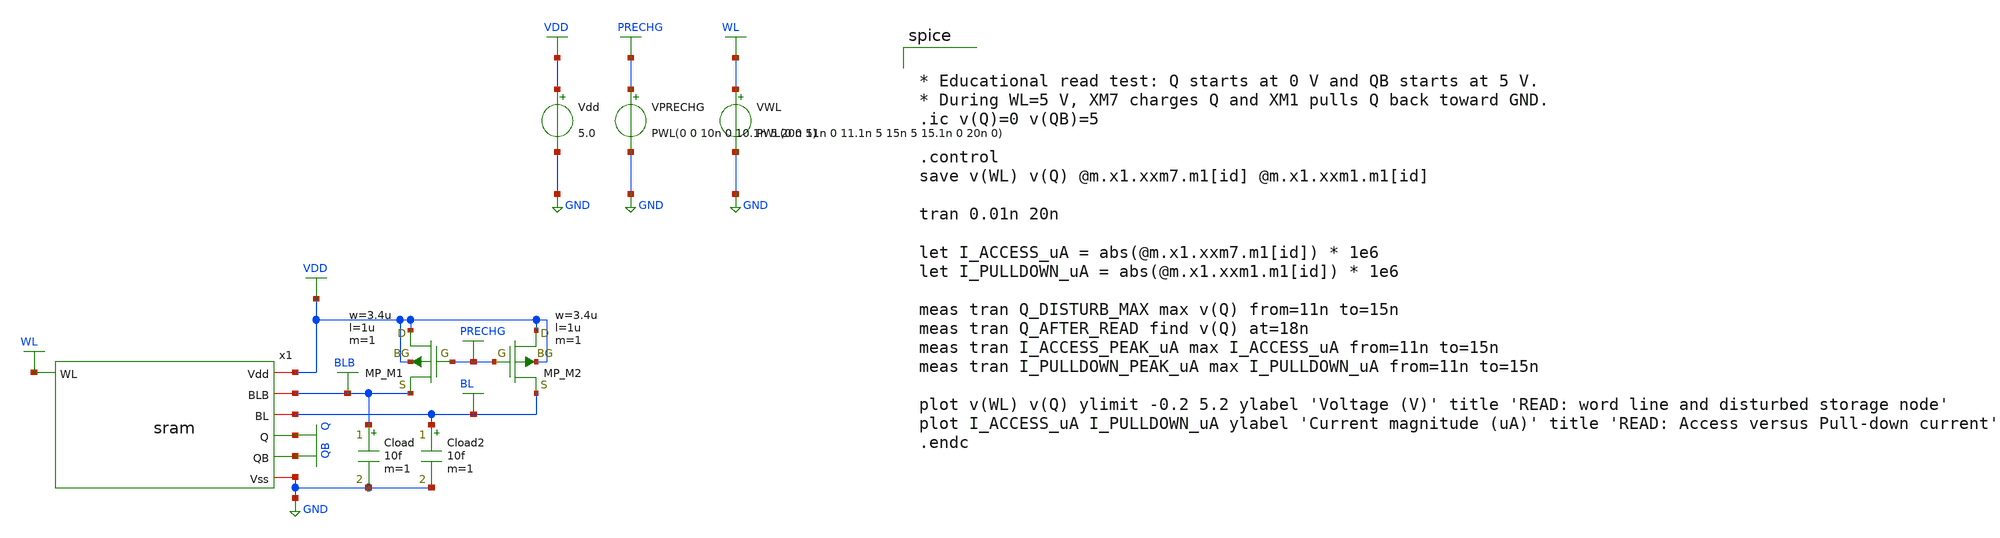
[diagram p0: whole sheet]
** sch_path: sram_tb_read_strength.sch
**.subckt sram_tb_read_strength
Vdd VDD GND 5.0
VWL WL GND PWL(0 0 11n 0 11.1n 5 15n 5 15.1n 0 20n 0)
x1 WL VDD BLB BL Q QB GND sram
XM1 VDD PRECHG BLB VDD PMOS w=3.4u l=1u as=0 ad=0 ps=0 pd=0 nrd=0 nrs=0 m=1
XM2 VDD PRECHG BL VDD PMOS w=3.4u l=1u as=0 ad=0 ps=0 pd=0 nrd=0 nrs=0 m=1
Cload BLB GND 10f m=1
Cload2 BL GND 10f m=1
VPRECHG PRECHG GND PWL(0 0 10n 0 10.1n 5 20n 5)
**** begin user architecture code
 .include $::LIB/ip62_models


* Educational read test: Q starts at 0 V and QB starts at 5 V.
* During WL=5 V, XM7 charges Q and XM1 pulls Q back toward GND.
.ic v(Q)=0 v(QB)=5

.control
save v(WL) v(Q) @m.x1.xxm7.m1[id] @m.x1.xxm1.m1[id]

tran 0.01n 20n

let I_ACCESS_uA = abs(@m.x1.xxm7.m1[id]) * 1e6
let I_PULLDOWN_uA = abs(@m.x1.xxm1.m1[id]) * 1e6

meas tran Q_DISTURB_MAX max v(Q) from=11n to=15n
meas tran Q_AFTER_READ find v(Q) at=18n
meas tran I_ACCESS_PEAK_uA max I_ACCESS_uA from=11n to=15n
meas tran I_PULLDOWN_PEAK_uA max I_PULLDOWN_uA from=11n to=15n

plot v(WL) v(Q) ylimit -0.2 5.2 ylabel 'Voltage (V)' title 'READ: word line and disturbed storage node'
plot I_ACCESS_uA I_PULLDOWN_uA ylabel 'Current magnitude (uA)' title 'READ: Access versus Pull-down current'
.endc


**** end user architecture code
**.ends

* expanding   symbol:  sram.sym # of pins=7
** sym_path: sram.sym
** sch_path: sram.sch
.subckt sram WL Vdd BLB BL Q QB Vss
*.iopin Vdd
*.iopin Vss
*.iopin BLB
*.iopin BL
*.ipin WL
*.opin Q
*.opin QB
XXM1 Q QB Vss Vss NMOS w=3.4u l=1u nrd=0 nrs=0 m=1
XXM2 Q QB Vdd Vdd PMOS w=3.4u l=1u nrd=0 nrs=0 m=1
XXM3 QB Q Vss Vss NMOS w=3.4u l=1u nrd=0 nrs=0 m=1
XXM4 QB Q Vdd Vdd PMOS w=3.4u l=1u nrd=0 nrs=0 m=1
XXM7 Q WL BL Vss NMOS w=3.4u l=1u nrd=0 nrs=0 m=1
XXM6 QB WL BLB Vss NMOS w=3.4u l=1u nrd=0 nrs=0 m=1
.ends

.GLOBAL VDD
.GLOBAL GND
.GLOBAL QB
.GLOBAL Q
.GLOBAL BLB
.GLOBAL WL
.GLOBAL BL
.GLOBAL PRECHG
.end
